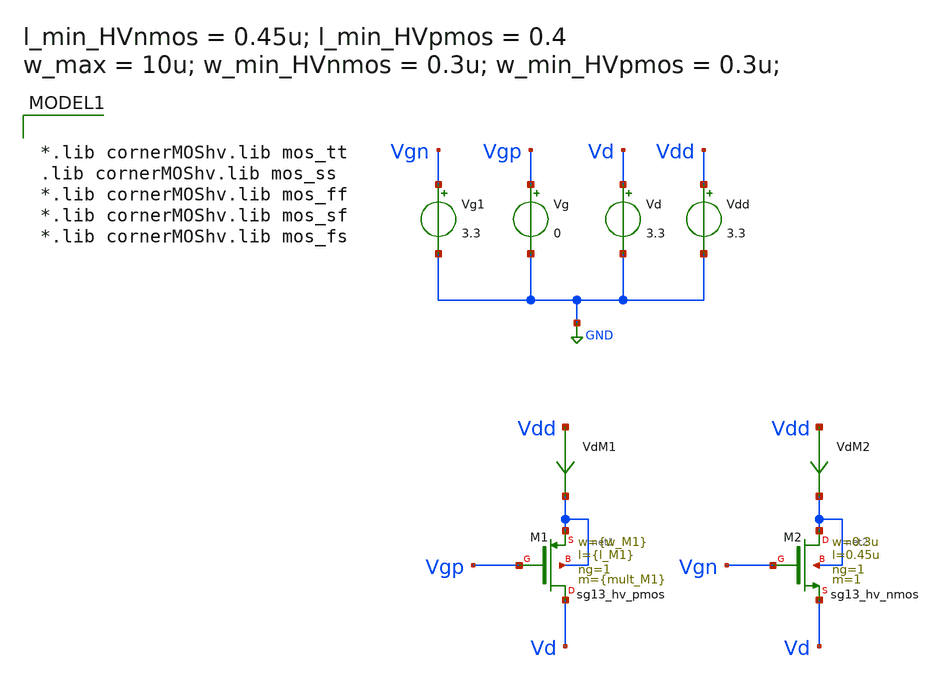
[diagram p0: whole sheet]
** sch_path: xschem/DCDCBuck/TB_hvPMOS_charact.sch
**.subckt TB_hvPMOS_charact
XM1 Vd Vgp net1 net1 sg13_hv_pmos w={w_M1} l={l_M1} ng=1 m={mult_M1} mm_ok=1
Vg Vgp GND 0
Vd Vd GND 3.3
Vdd Vdd GND 3.3
VdM1 Vdd net1 0
.save i(vdm1)
VdM2 Vdd net2 0
.save i(vdm2)
XM2 net2 Vgn Vd net2 sg13_hv_nmos w=0.3u l=0.45u ng=1 m=1 mm_ok=1
Vg1 Vgn GND 3.3
**** begin user architecture code


.param mult_M1 = 1200
.param w_M1 = 10u
.param l_M1 = 0.45u

.param mult_M2 = 1200
.param w_M2 = 10u
.param l_M2 = 0.45u

.save all  @n.xm1.nsg13_hv_pmos[vth]  @n.xm1.nsg13_hv_pmos[gds]  @n.xm2.nsg13_hv_nmos[vth]  @n.xm2.nsg13_hv_nmos[gds]

.control
dc Vd 0 3.3 0.01

let Vsd = v(Vdd) - v(Vd)
let G_M1 = @n.xm1.nsg13_hv_pmos[gds]
let G_M2 = @n.xm2.nsg13_hv_nmos[gds]
let Ron_M1 = 1/G_M1
let Ron_M2 = 1/G_M2

plot i(VdM1) i(VdM2) vs Vsd
plot Ron_M1 Ron_M2 vs Vsd
write test_pmos.raw
.endc

.control
reset
alter Vd 0
dc Vg 2 3.3 0.01
let Vsg = v(Vdd) - v(Vg)
plot i(VdM1) i(VdM2) i(VdM3) vs Vsg
.endc




*.lib cornerMOShv.lib mos_tt
.lib cornerMOShv.lib mos_ss
*.lib cornerMOShv.lib mos_ff
*.lib cornerMOShv.lib mos_sf
*.lib cornerMOShv.lib mos_fs

**** end user architecture code
**.ends
.GLOBAL GND
.end
